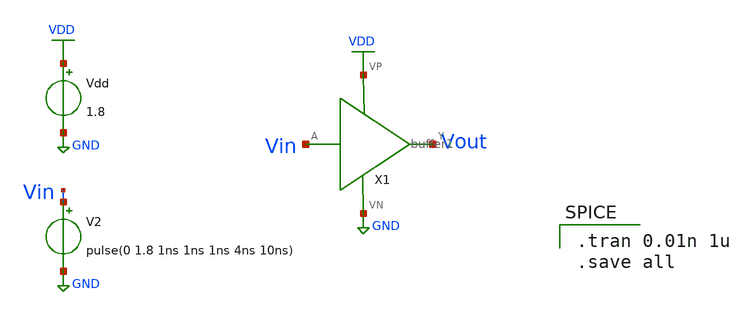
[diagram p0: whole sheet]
** sch_path: Buffer_Hierarchy/buffer_tran.sch
**.subckt buffer_tran
Vdd VDD GND 1.8
V2 Vin GND pulse(0 1.8 1ns 1ns 1ns 4ns 10ns)
X1 Vin VDD GND Vout buffer1
**** begin user architecture code

** opencircuitdesign pdks install
.lib $::SKYWATER_MODELS/sky130.lib.spice tt


.tran 0.01n 1u
.save all

**** end user architecture code
**.ends
.GLOBAL VDD
.GLOBAL GND
.end
